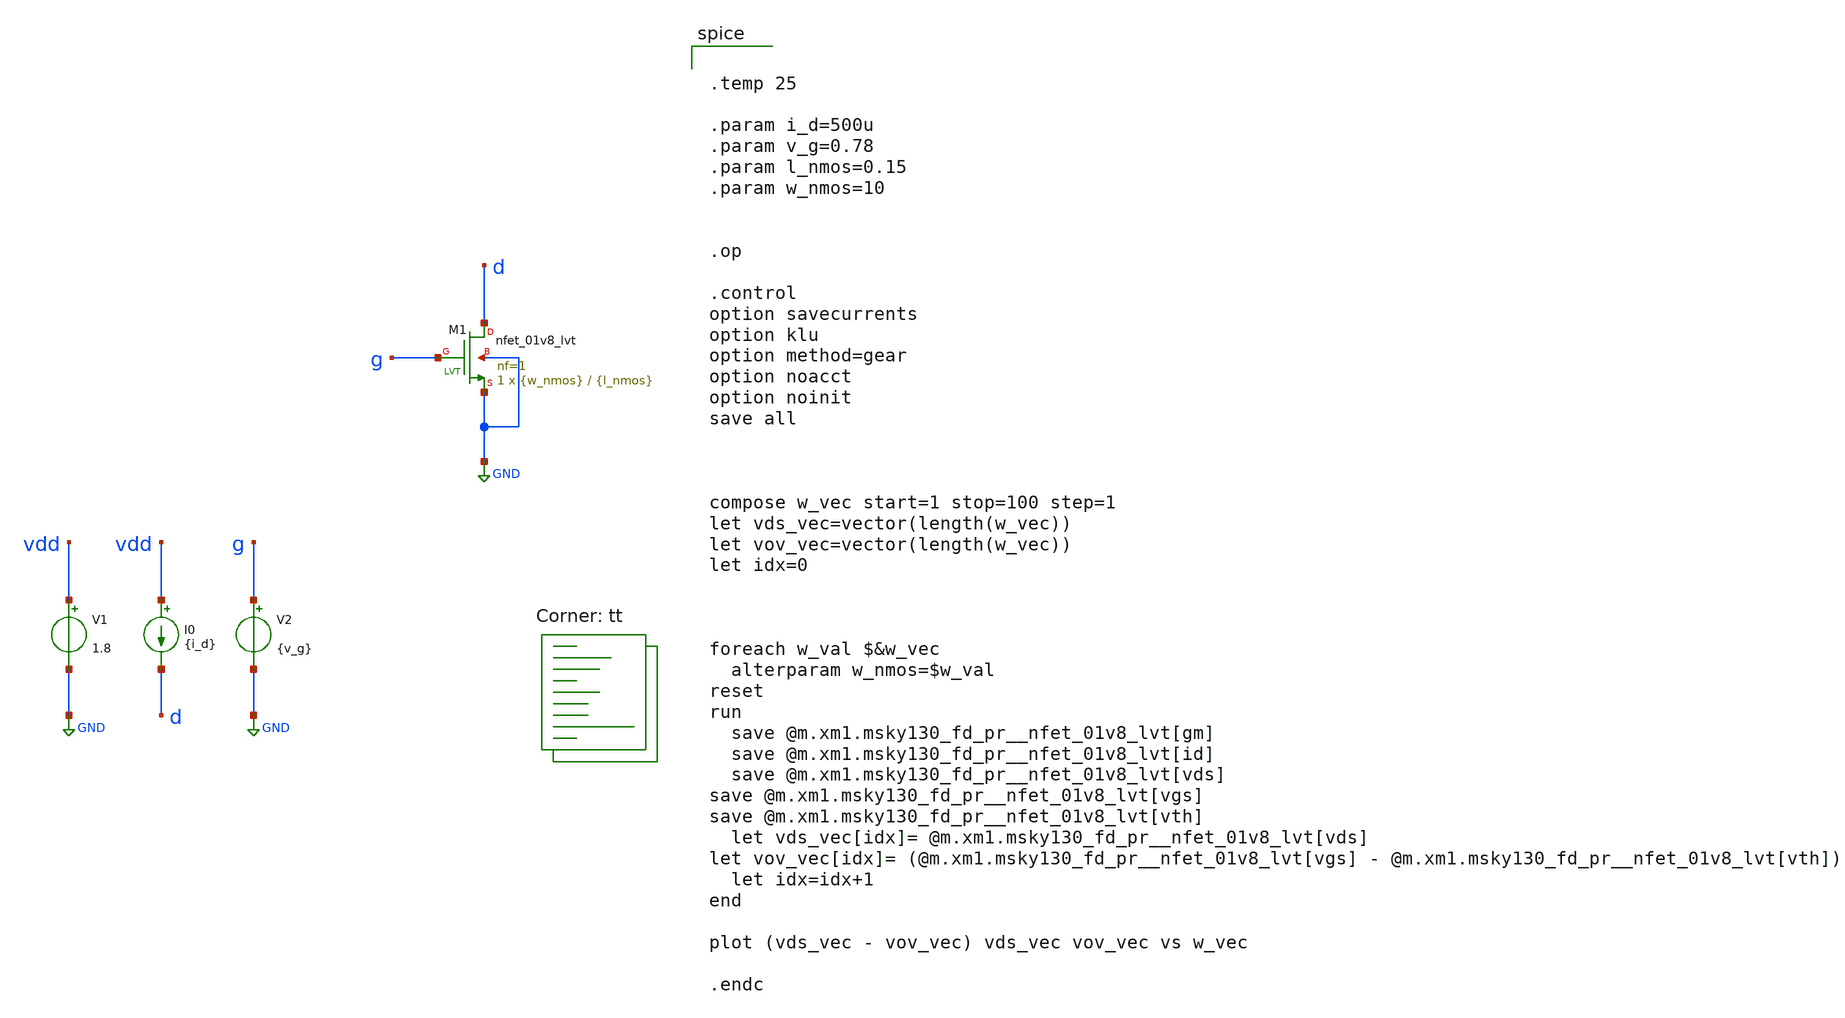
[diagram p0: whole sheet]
** sch_path: xschem/nmos_id_vgs.sch
**.subckt nmos_id_vgs
V1 vdd GND 1.8
.save i(v1)
XM1 d g GND GND sky130_fd_pr__nfet_01v8_lvt L={l_nmos} W={w_nmos} nf=1 ad='int((1 + 1)/2) * {w_nmos} / 1 * 0.29'
+ as='int((1 + 2)/2) * {w_nmos} / 1 * 0.29' pd='2*int((1 + 1)/2) * ({w_nmos} / 1 + 0.29)' ps='2*int((1 + 2)/2) * ({w_nmos} / 1 + 0.29)'
+ nrd='0.29 / {w_nmos} ' nrs='0.29 / {w_nmos} ' sa=0 sb=0 sd=0 mult=1 m=1
I0 vdd d {i_d}
V2 g GND {v_g}
.save i(v2)
**** begin user architecture code
.lib $::SKYWATER_MODELS/sky130.lib.spice tt


.temp 25

.param i_d=500u
.param v_g=0.78
.param l_nmos=0.15
.param w_nmos=10


.op

.control
option savecurrents
option klu
option method=gear
option noacct
option noinit
save all



compose w_vec start=1 stop=100 step=1
let vds_vec=vector(length(w_vec))
let vov_vec=vector(length(w_vec))
let idx=0



foreach w_val $&w_vec
  alterparam w_nmos=$w_val
reset
run
  save @m.xm1.msky130_fd_pr__nfet_01v8_lvt[gm]
  save @m.xm1.msky130_fd_pr__nfet_01v8_lvt[id]
  save @m.xm1.msky130_fd_pr__nfet_01v8_lvt[vds]
save @m.xm1.msky130_fd_pr__nfet_01v8_lvt[vgs]
save @m.xm1.msky130_fd_pr__nfet_01v8_lvt[vth]
  let vds_vec[idx]= @m.xm1.msky130_fd_pr__nfet_01v8_lvt[vds]
let vov_vec[idx]= (@m.xm1.msky130_fd_pr__nfet_01v8_lvt[vgs] -
+ @m.xm1.msky130_fd_pr__nfet_01v8_lvt[vth])
  let idx=idx+1
end

plot (vds_vec - vov_vec) vds_vec vov_vec vs w_vec

.endc

**** end user architecture code
**.ends
.GLOBAL GND
.end
